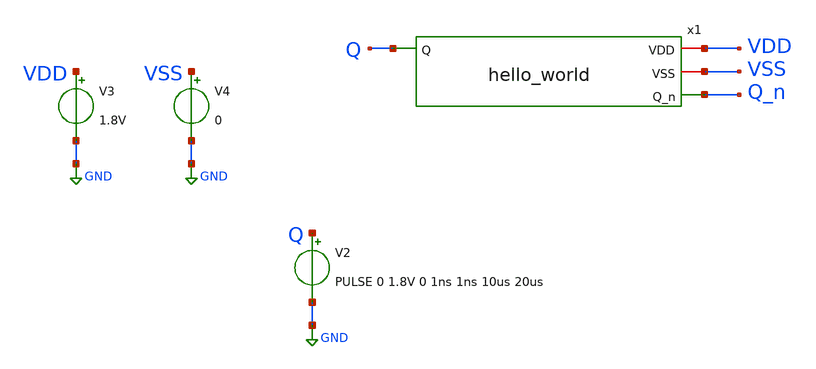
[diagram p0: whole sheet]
** sch_path: xschem/hello_world_test.sch
**.subckt hello_world_test
x1 Q VDD VSS Q_n hello_world
V3 VDD GND 1.8V
V4 VSS GND 0
V2 Q GND PULSE 0 1.8V 0 1ns 1ns 10us 20us
**** begin user architecture code
 .lib $::SKYWATER_MODELS/sky130.lib.spice tt
.include $::SKYWATER_STDCELLS/sky130_fd_sc_hd.spice


.options acct list
.temp 25
*vvcc VDD 0 dc 1.8
*vvss VSS 0 0
.control
*tran 0.1u 60u
dc V2 0 1.8 1m
*plot RST_PLS clk+2 Pulse+4
plot Q Q_n
write hello_world_test.raw
.endc


**** end user architecture code
**.ends

* expanding   symbol:  hello_world.sym # of pins=4
** sym_path: xschem/hello_world.sym
** sch_path: xschem/hello_world.sch
.subckt hello_world Q VDD VSS Q_n
*.ipin Q
*.opin Q_n
*.iopin VDD
*.iopin VSS
XM1 Q_n Q VDD VSS sky130_fd_pr__pfet_01v8 L=0.15 W=2 nf=1 ad='int((nf+1)/2) * W/nf * 0.29' as='int((nf+2)/2) * W/nf * 0.29'
+ pd='2*int((nf+1)/2) * (W/nf + 0.29)' ps='2*int((nf+2)/2) * (W/nf + 0.29)' nrd='0.29 / W' nrs='0.29 / W'
+ sa=0 sb=0 sd=0 mult=4 m=4
XM2 Q_n Q VSS VSS sky130_fd_pr__nfet_01v8 L=0.15 W=1 nf=1 ad='int((nf+1)/2) * W/nf * 0.29' as='int((nf+2)/2) * W/nf * 0.29'
+ pd='2*int((nf+1)/2) * (W/nf + 0.29)' ps='2*int((nf+2)/2) * (W/nf + 0.29)' nrd='0.29 / W' nrs='0.29 / W'
+ sa=0 sb=0 sd=0 mult=4 m=4
.ends

.GLOBAL GND
.end
